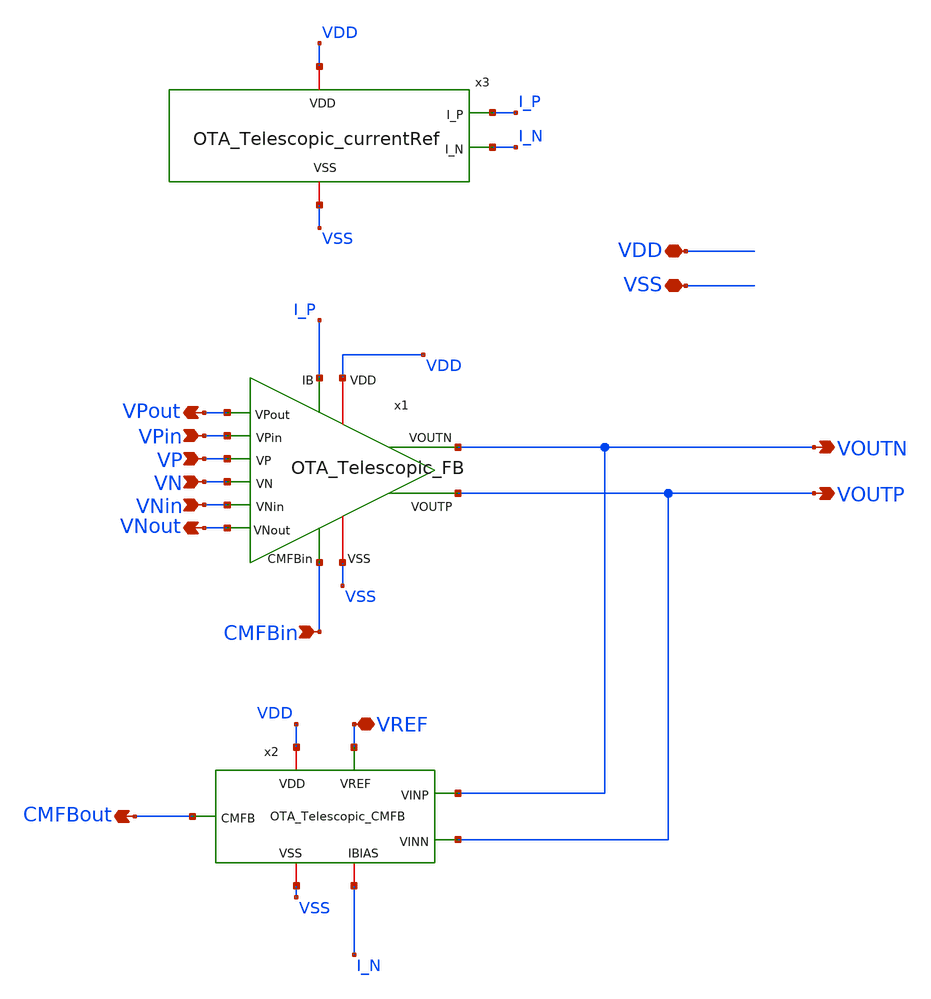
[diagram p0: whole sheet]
** sch_path: OTA_Telescopic_NO_FLATTEN/Schematics_and_Symbols/OTA_Telescopic_TOP_wp.sch
**.subckt OTA_Telescopic_TOP_wp VP VN VOUTP VOUTN VPin VNin VPout VNout VDD VSS VREF CMFBin CMFBout
*.ipin VP
*.ipin VN
*.opin VOUTP
*.opin VOUTN
*.ipin VPin
*.ipin VNin
*.opin VPout
*.opin VNout
*.iopin VDD
*.iopin VSS
*.iopin VREF
*.ipin CMFBin
*.opin CMFBout
x3 VDD I_P I_N VSS OTA_Telescopic_currentRef
x2 VDD VREF VOUTP VOUTN I_N CMFBout VSS OTA_Telescopic_CMFB
x1 I_P VPout VP VPin VOUTP VDD VOUTN VSS VNin VNout VN CMFBin OTA_Telescopic_FB
**.ends
.end
